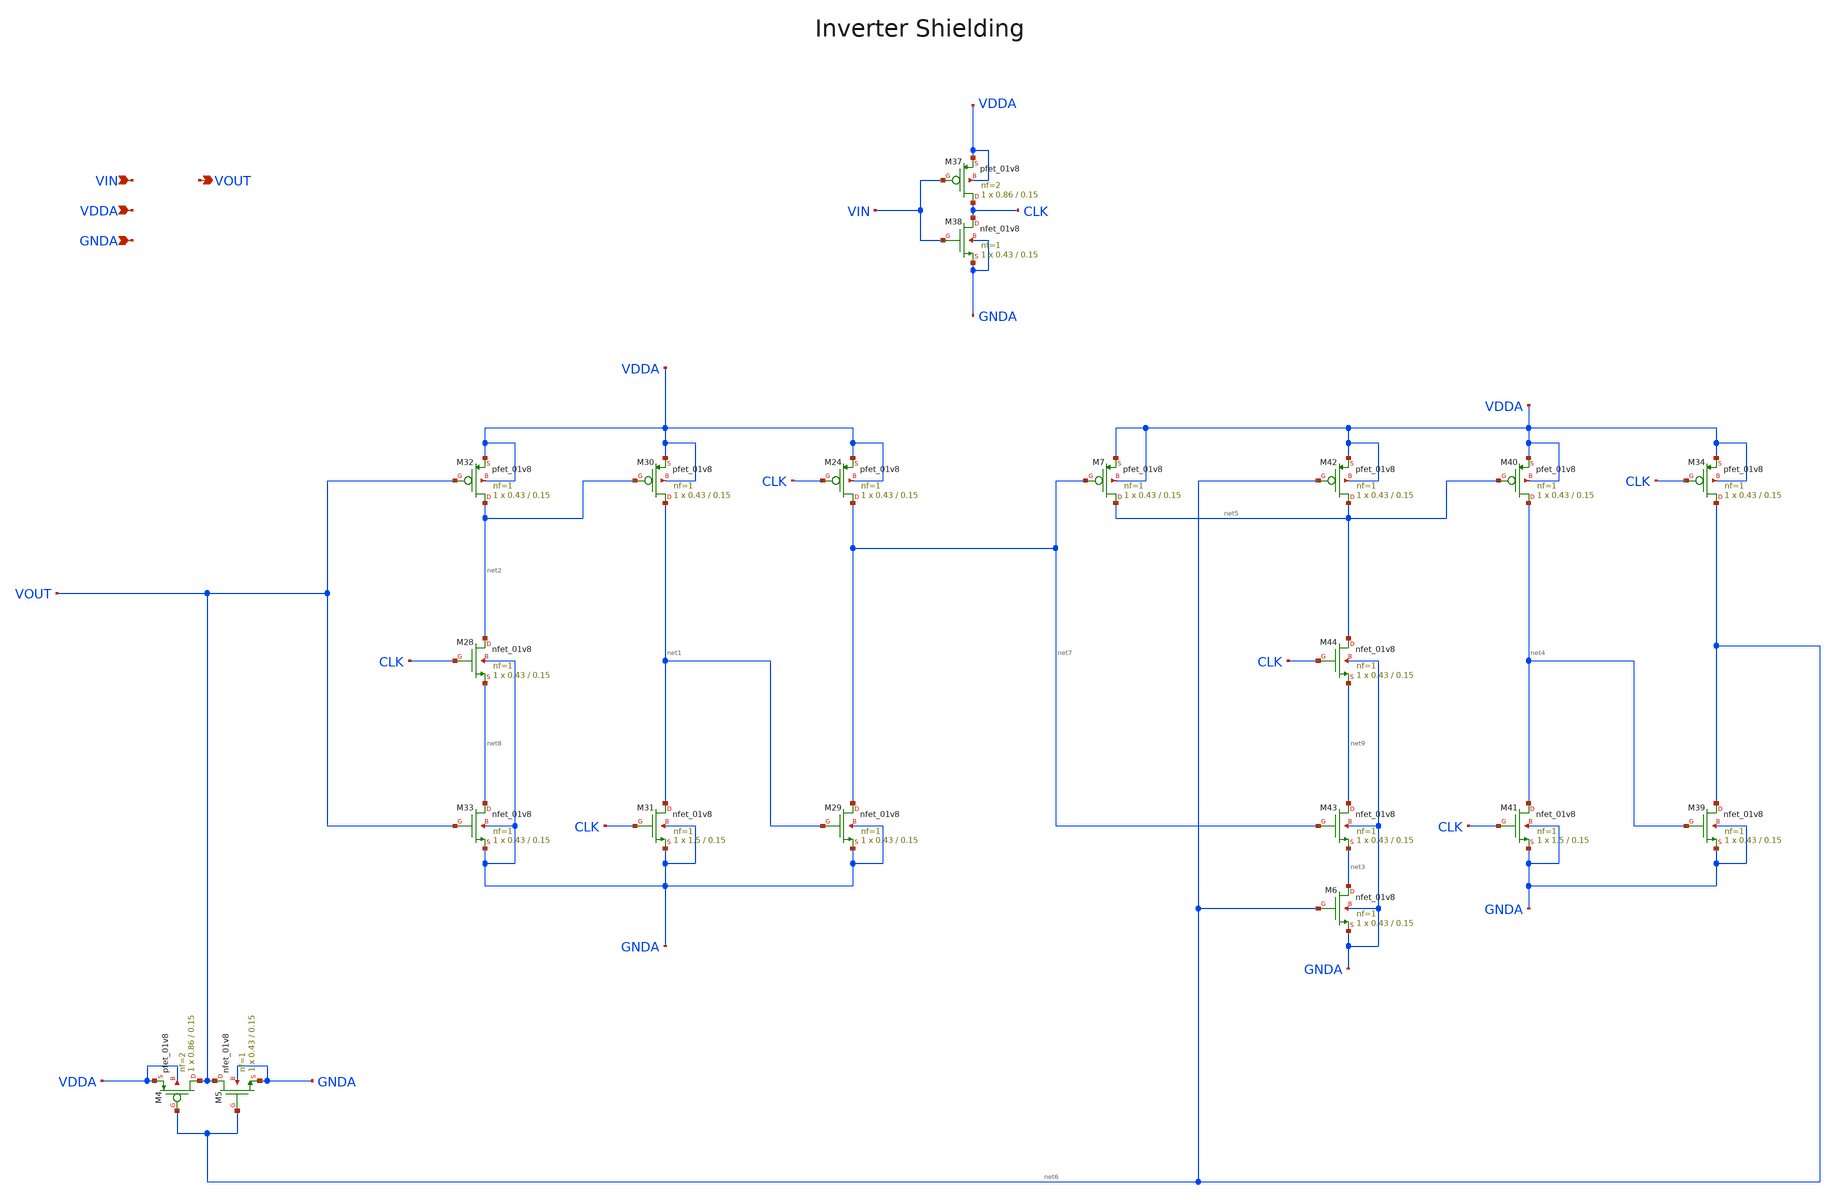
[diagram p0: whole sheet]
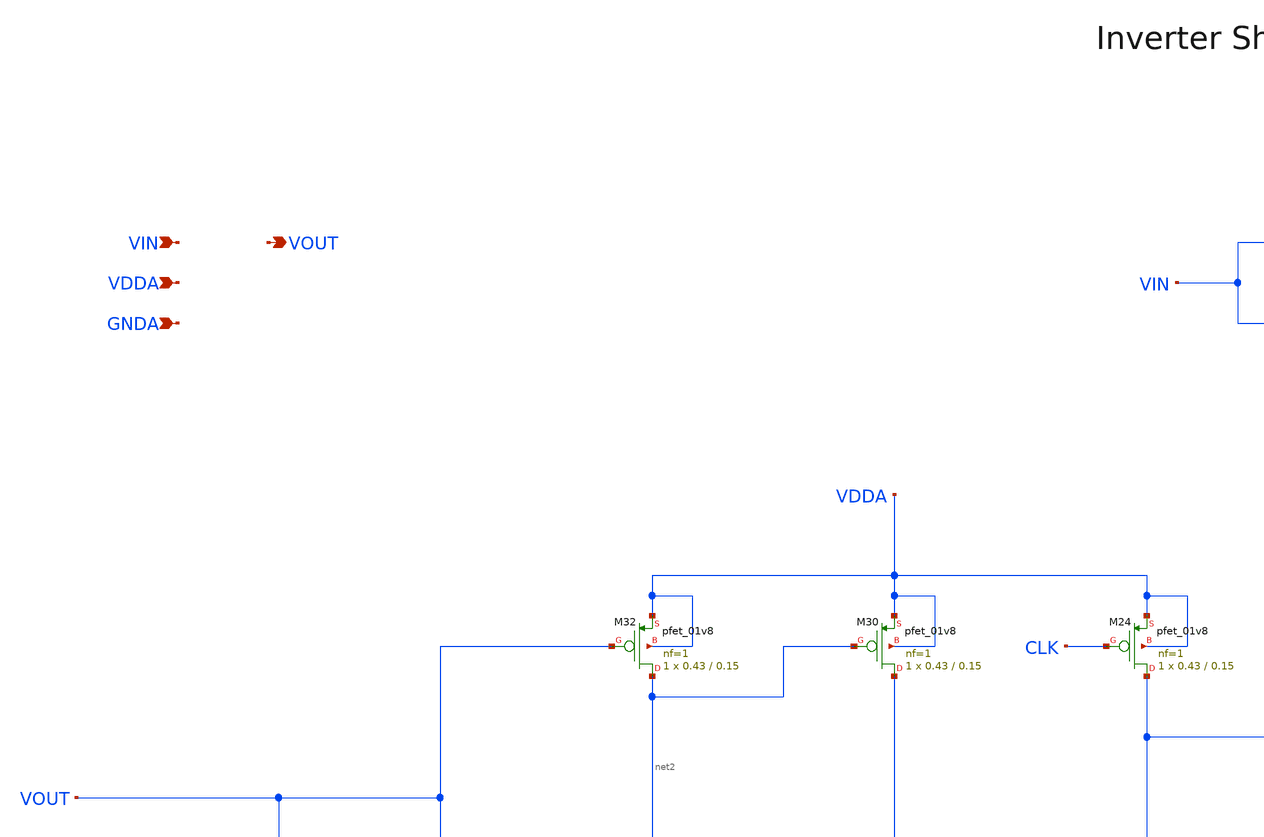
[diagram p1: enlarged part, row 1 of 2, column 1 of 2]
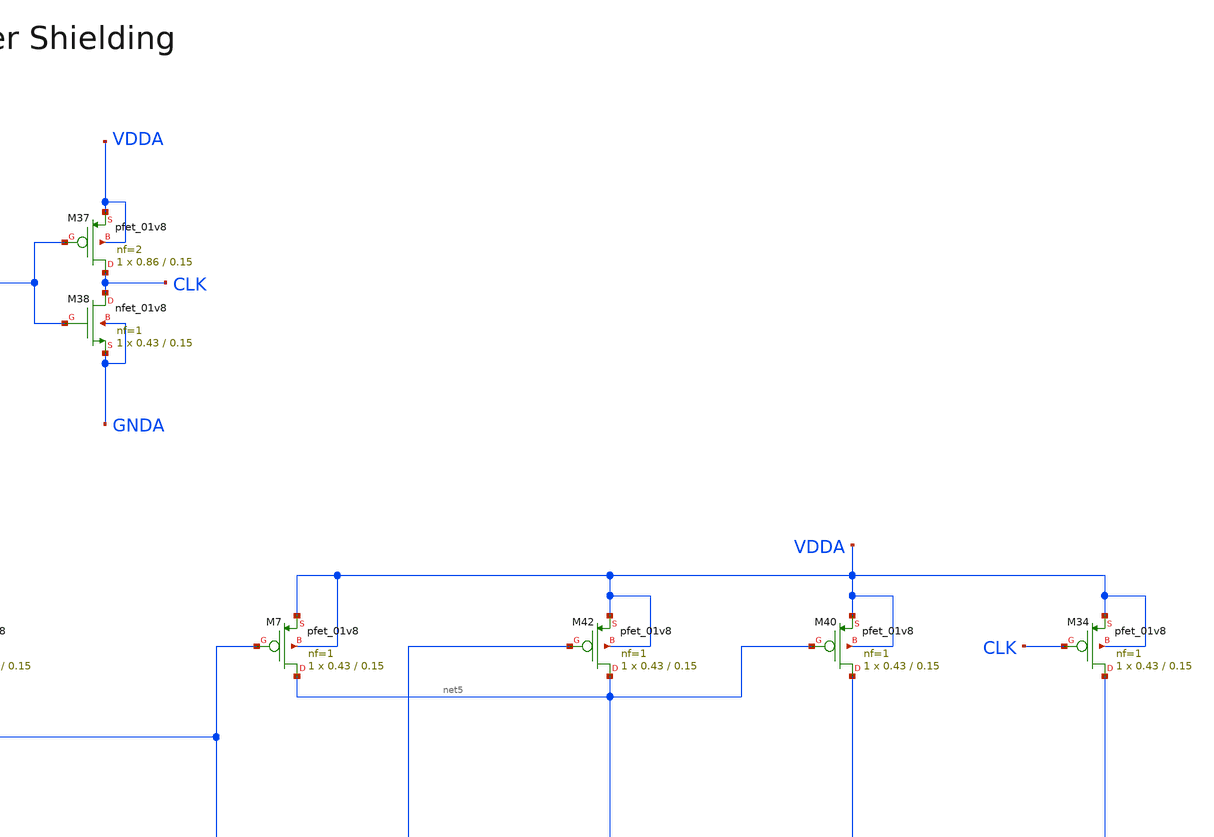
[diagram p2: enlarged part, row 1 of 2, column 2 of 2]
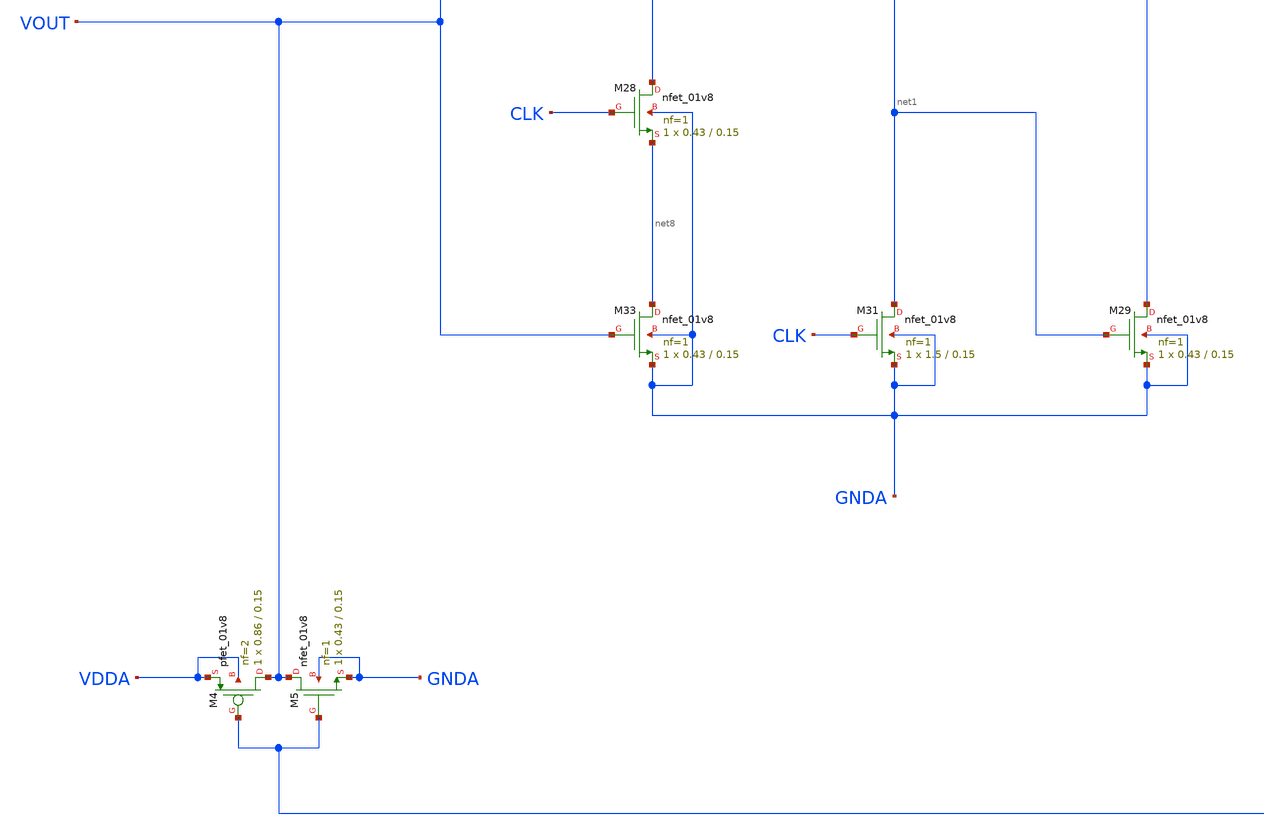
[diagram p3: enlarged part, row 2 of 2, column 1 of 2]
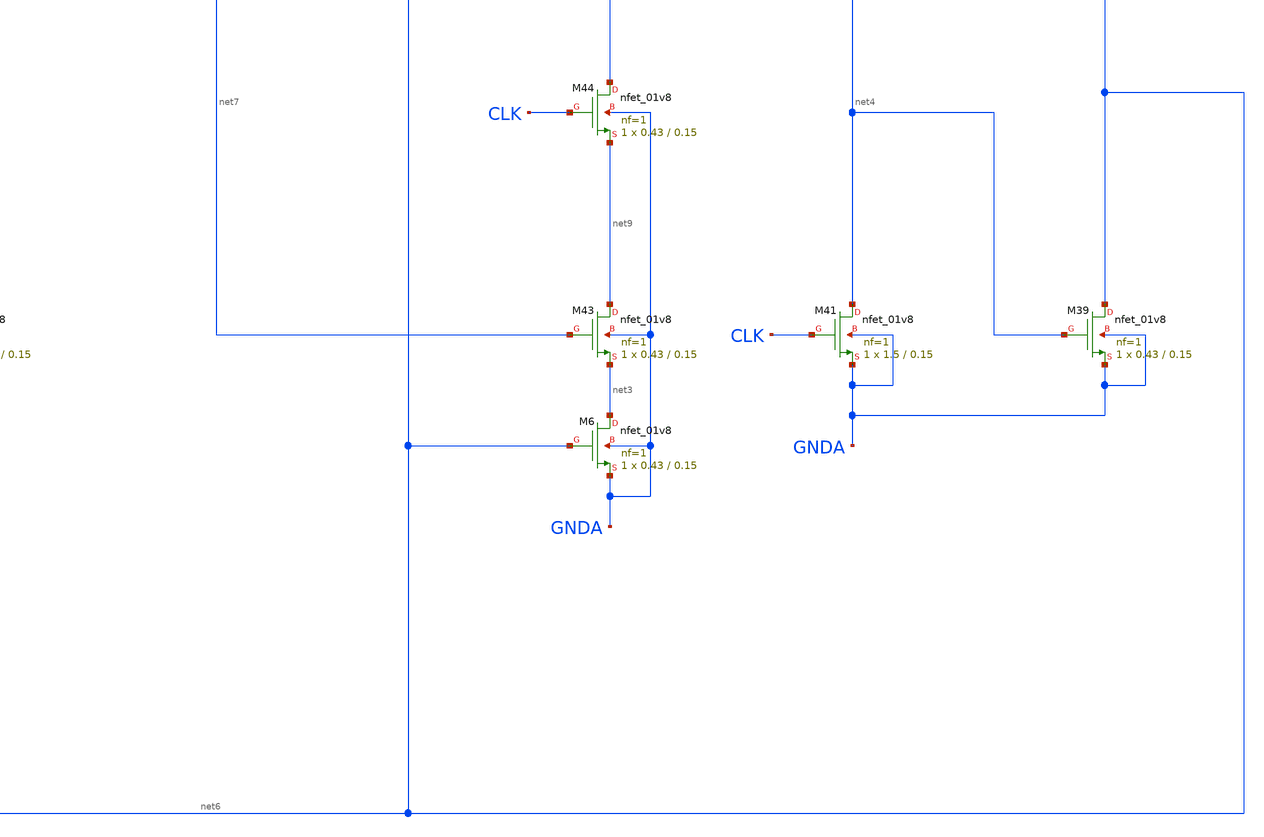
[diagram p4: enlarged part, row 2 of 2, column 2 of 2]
** sch_path: projects/pll/divider/xschem_ngspice/TSPC_FF_ratioed_divide3_2.sch
**.subckt TSPC_FF_ratioed_divide3_2 VIN VOUT VDDA GNDA
*.ipin VIN
*.opin VOUT
*.ipin VDDA
*.ipin GNDA
XM24 net7 CLK VDDA VDDA sky130_fd_pr__pfet_01v8 L=0.15 W=0.43 nf=1 ad='int((nf+1)/2) * W/nf * 0.29' as='int((nf+2)/2) * W/nf * 0.29'
+ pd='2*int((nf+1)/2) * (W/nf + 0.29)' ps='2*int((nf+2)/2) * (W/nf + 0.29)' nrd='0.29 / W' nrs='0.29 / W'
+ sa=0 sb=0 sd=0 mult=1 m=1
XM29 net7 net1 GNDA GNDA sky130_fd_pr__nfet_01v8 L=0.15 W=0.43 nf=1 ad='int((nf+1)/2) * W/nf * 0.29'
+ as='int((nf+2)/2) * W/nf * 0.29' pd='2*int((nf+1)/2) * (W/nf + 0.29)' ps='2*int((nf+2)/2) * (W/nf + 0.29)'
+ nrd='0.29 / W' nrs='0.29 / W' sa=0 sb=0 sd=0 mult=1 m=1
XM30 net1 net2 VDDA VDDA sky130_fd_pr__pfet_01v8 L=0.15 W=0.43 nf=1 ad='int((nf+1)/2) * W/nf * 0.29'
+ as='int((nf+2)/2) * W/nf * 0.29' pd='2*int((nf+1)/2) * (W/nf + 0.29)' ps='2*int((nf+2)/2) * (W/nf + 0.29)'
+ nrd='0.29 / W' nrs='0.29 / W' sa=0 sb=0 sd=0 mult=1 m=1
XM31 net1 CLK GNDA GNDA sky130_fd_pr__nfet_01v8 L=0.15 W=1.5 nf=1 ad='int((nf+1)/2) * W/nf * 0.29' as='int((nf+2)/2) * W/nf * 0.29'
+ pd='2*int((nf+1)/2) * (W/nf + 0.29)' ps='2*int((nf+2)/2) * (W/nf + 0.29)' nrd='0.29 / W' nrs='0.29 / W'
+ sa=0 sb=0 sd=0 mult=1 m=1
XM32 net2 VOUT VDDA VDDA sky130_fd_pr__pfet_01v8 L=0.15 W=0.43 nf=1 ad='int((nf+1)/2) * W/nf * 0.29'
+ as='int((nf+2)/2) * W/nf * 0.29' pd='2*int((nf+1)/2) * (W/nf + 0.29)' ps='2*int((nf+2)/2) * (W/nf + 0.29)'
+ nrd='0.29 / W' nrs='0.29 / W' sa=0 sb=0 sd=0 mult=1 m=1
XM33 net8 VOUT GNDA GNDA sky130_fd_pr__nfet_01v8 L=0.15 W=0.43 nf=1 ad='int((nf+1)/2) * W/nf * 0.29'
+ as='int((nf+2)/2) * W/nf * 0.29' pd='2*int((nf+1)/2) * (W/nf + 0.29)' ps='2*int((nf+2)/2) * (W/nf + 0.29)'
+ nrd='0.29 / W' nrs='0.29 / W' sa=0 sb=0 sd=0 mult=1 m=1
XM28 net2 CLK net8 GNDA sky130_fd_pr__nfet_01v8 L=0.15 W=0.43 nf=1 ad='int((nf+1)/2) * W/nf * 0.29' as='int((nf+2)/2) * W/nf * 0.29'
+ pd='2*int((nf+1)/2) * (W/nf + 0.29)' ps='2*int((nf+2)/2) * (W/nf + 0.29)' nrd='0.29 / W' nrs='0.29 / W'
+ sa=0 sb=0 sd=0 mult=1 m=1
XM34 net6 CLK VDDA VDDA sky130_fd_pr__pfet_01v8 L=0.15 W=0.43 nf=1 ad='int((nf+1)/2) * W/nf * 0.29' as='int((nf+2)/2) * W/nf * 0.29'
+ pd='2*int((nf+1)/2) * (W/nf + 0.29)' ps='2*int((nf+2)/2) * (W/nf + 0.29)' nrd='0.29 / W' nrs='0.29 / W'
+ sa=0 sb=0 sd=0 mult=1 m=1
XM39 net6 net4 GNDA GNDA sky130_fd_pr__nfet_01v8 L=0.15 W=0.43 nf=1 ad='int((nf+1)/2) * W/nf * 0.29'
+ as='int((nf+2)/2) * W/nf * 0.29' pd='2*int((nf+1)/2) * (W/nf + 0.29)' ps='2*int((nf+2)/2) * (W/nf + 0.29)'
+ nrd='0.29 / W' nrs='0.29 / W' sa=0 sb=0 sd=0 mult=1 m=1
XM40 net4 net5 VDDA VDDA sky130_fd_pr__pfet_01v8 L=0.15 W=0.43 nf=1 ad='int((nf+1)/2) * W/nf * 0.29'
+ as='int((nf+2)/2) * W/nf * 0.29' pd='2*int((nf+1)/2) * (W/nf + 0.29)' ps='2*int((nf+2)/2) * (W/nf + 0.29)'
+ nrd='0.29 / W' nrs='0.29 / W' sa=0 sb=0 sd=0 mult=1 m=1
XM41 net4 CLK GNDA GNDA sky130_fd_pr__nfet_01v8 L=0.15 W=1.5 nf=1 ad='int((nf+1)/2) * W/nf * 0.29' as='int((nf+2)/2) * W/nf * 0.29'
+ pd='2*int((nf+1)/2) * (W/nf + 0.29)' ps='2*int((nf+2)/2) * (W/nf + 0.29)' nrd='0.29 / W' nrs='0.29 / W'
+ sa=0 sb=0 sd=0 mult=1 m=1
XM42 net5 net6 VDDA VDDA sky130_fd_pr__pfet_01v8 L=0.15 W=0.43 nf=1 ad='int((nf+1)/2) * W/nf * 0.29'
+ as='int((nf+2)/2) * W/nf * 0.29' pd='2*int((nf+1)/2) * (W/nf + 0.29)' ps='2*int((nf+2)/2) * (W/nf + 0.29)'
+ nrd='0.29 / W' nrs='0.29 / W' sa=0 sb=0 sd=0 mult=1 m=1
XM43 net9 net7 net3 GNDA sky130_fd_pr__nfet_01v8 L=0.15 W=0.43 nf=1 ad='int((nf+1)/2) * W/nf * 0.29'
+ as='int((nf+2)/2) * W/nf * 0.29' pd='2*int((nf+1)/2) * (W/nf + 0.29)' ps='2*int((nf+2)/2) * (W/nf + 0.29)'
+ nrd='0.29 / W' nrs='0.29 / W' sa=0 sb=0 sd=0 mult=1 m=1
XM44 net5 CLK net9 GNDA sky130_fd_pr__nfet_01v8 L=0.15 W=0.43 nf=1 ad='int((nf+1)/2) * W/nf * 0.29' as='int((nf+2)/2) * W/nf * 0.29'
+ pd='2*int((nf+1)/2) * (W/nf + 0.29)' ps='2*int((nf+2)/2) * (W/nf + 0.29)' nrd='0.29 / W' nrs='0.29 / W'
+ sa=0 sb=0 sd=0 mult=1 m=1
XM4 VOUT net6 VDDA VDDA sky130_fd_pr__pfet_01v8 L=0.15 W=0.86 nf=2 ad='int((nf+1)/2) * W/nf * 0.29' as='int((nf+2)/2) * W/nf * 0.29'
+ pd='2*int((nf+1)/2) * (W/nf + 0.29)' ps='2*int((nf+2)/2) * (W/nf + 0.29)' nrd='0.29 / W' nrs='0.29 / W'
+ sa=0 sb=0 sd=0 mult=1 m=1
XM5 VOUT net6 GNDA GNDA sky130_fd_pr__nfet_01v8 L=0.15 W=0.43 nf=1 ad='int((nf+1)/2) * W/nf * 0.29' as='int((nf+2)/2) * W/nf * 0.29'
+ pd='2*int((nf+1)/2) * (W/nf + 0.29)' ps='2*int((nf+2)/2) * (W/nf + 0.29)' nrd='0.29 / W' nrs='0.29 / W'
+ sa=0 sb=0 sd=0 mult=1 m=1
XM6 net3 net6 GNDA GNDA sky130_fd_pr__nfet_01v8 L=0.15 W=0.43 nf=1 ad='int((nf+1)/2) * W/nf * 0.29' as='int((nf+2)/2) * W/nf * 0.29'
+ pd='2*int((nf+1)/2) * (W/nf + 0.29)' ps='2*int((nf+2)/2) * (W/nf + 0.29)' nrd='0.29 / W' nrs='0.29 / W'
+ sa=0 sb=0 sd=0 mult=1 m=1
XM7 net5 net7 VDDA VDDA sky130_fd_pr__pfet_01v8 L=0.15 W=0.43 nf=1 ad='int((nf+1)/2) * W/nf * 0.29' as='int((nf+2)/2) * W/nf * 0.29'
+ pd='2*int((nf+1)/2) * (W/nf + 0.29)' ps='2*int((nf+2)/2) * (W/nf + 0.29)' nrd='0.29 / W' nrs='0.29 / W'
+ sa=0 sb=0 sd=0 mult=1 m=1
XM37 CLK VIN VDDA VDDA sky130_fd_pr__pfet_01v8 L=0.15 W=0.86 nf=2 ad='int((nf+1)/2) * W/nf * 0.29' as='int((nf+2)/2) * W/nf * 0.29'
+ pd='2*int((nf+1)/2) * (W/nf + 0.29)' ps='2*int((nf+2)/2) * (W/nf + 0.29)' nrd='0.29 / W' nrs='0.29 / W'
+ sa=0 sb=0 sd=0 mult=1 m=1
XM38 CLK VIN GNDA GNDA sky130_fd_pr__nfet_01v8 L=0.15 W=0.43 nf=1 ad='int((nf+1)/2) * W/nf * 0.29' as='int((nf+2)/2) * W/nf * 0.29'
+ pd='2*int((nf+1)/2) * (W/nf + 0.29)' ps='2*int((nf+2)/2) * (W/nf + 0.29)' nrd='0.29 / W' nrs='0.29 / W'
+ sa=0 sb=0 sd=0 mult=1 m=1
**.ends
.end
